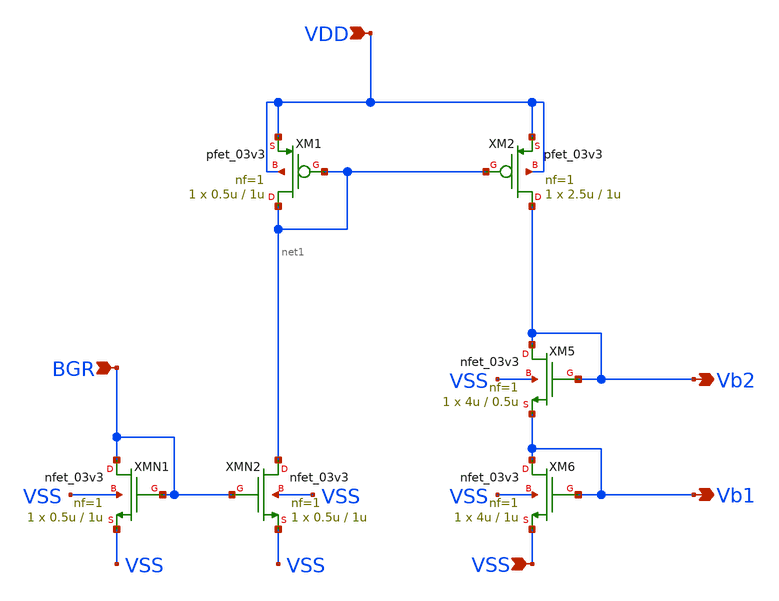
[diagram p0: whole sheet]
** sch_path: DAC/xschem/dac_current_mirror.sch
**.subckt dac_current_mirror BGR VDD VSS Vb2 Vb1
*.ipin BGR
*.ipin VDD
*.ipin VSS
*.opin Vb2
*.opin Vb1
XM1 net1 net1 VDD VDD pfet_03v3 L=1u W=0.5u nf=1 ad='int((nf+1)/2) * W/nf * 0.18u' as='int((nf+2)/2) * W/nf * 0.18u'
+ pd='2*int((nf+1)/2) * (W/nf + 0.18u)' ps='2*int((nf+2)/2) * (W/nf + 0.18u)' nrd='0.18u / W' nrs='0.18u / W'
+ sa=0 sb=0 sd=0 m=1
XM2 Vb2 net1 VDD VDD pfet_03v3 L=1u W=2.5u nf=1 ad='int((nf+1)/2) * W/nf * 0.18u' as='int((nf+2)/2) * W/nf * 0.18u'
+ pd='2*int((nf+1)/2) * (W/nf + 0.18u)' ps='2*int((nf+2)/2) * (W/nf + 0.18u)' nrd='0.18u / W' nrs='0.18u / W'
+ sa=0 sb=0 sd=0 m=1
XMN1 BGR BGR VSS VSS nfet_03v3 L=1u W=0.5u nf=1 ad='int((nf+1)/2) * W/nf * 0.18u' as='int((nf+2)/2) * W/nf * 0.18u'
+ pd='2*int((nf+1)/2) * (W/nf + 0.18u)' ps='2*int((nf+2)/2) * (W/nf + 0.18u)' nrd='0.18u / W' nrs='0.18u / W'
+ sa=0 sb=0 sd=0 m=1
XMN2 net1 BGR VSS VSS nfet_03v3 L=1u W=0.5u nf=1 ad='int((nf+1)/2) * W/nf * 0.18u' as='int((nf+2)/2) * W/nf * 0.18u'
+ pd='2*int((nf+1)/2) * (W/nf + 0.18u)' ps='2*int((nf+2)/2) * (W/nf + 0.18u)' nrd='0.18u / W' nrs='0.18u / W'
+ sa=0 sb=0 sd=0 m=1
XM5 Vb2 Vb2 Vb1 VSS nfet_03v3 L=0.5u W=4u nf=1 ad='int((nf+1)/2) * W/nf * 0.18u' as='int((nf+2)/2) * W/nf * 0.18u'
+ pd='2*int((nf+1)/2) * (W/nf + 0.18u)' ps='2*int((nf+2)/2) * (W/nf + 0.18u)' nrd='0.18u / W' nrs='0.18u / W'
+ sa=0 sb=0 sd=0 m=1
XM6 Vb1 Vb1 VSS VSS nfet_03v3 L=1u W=4u nf=1 ad='int((nf+1)/2) * W/nf * 0.18u' as='int((nf+2)/2) * W/nf * 0.18u'
+ pd='2*int((nf+1)/2) * (W/nf + 0.18u)' ps='2*int((nf+2)/2) * (W/nf + 0.18u)' nrd='0.18u / W' nrs='0.18u / W'
+ sa=0 sb=0 sd=0 m=1
**.ends
.end
